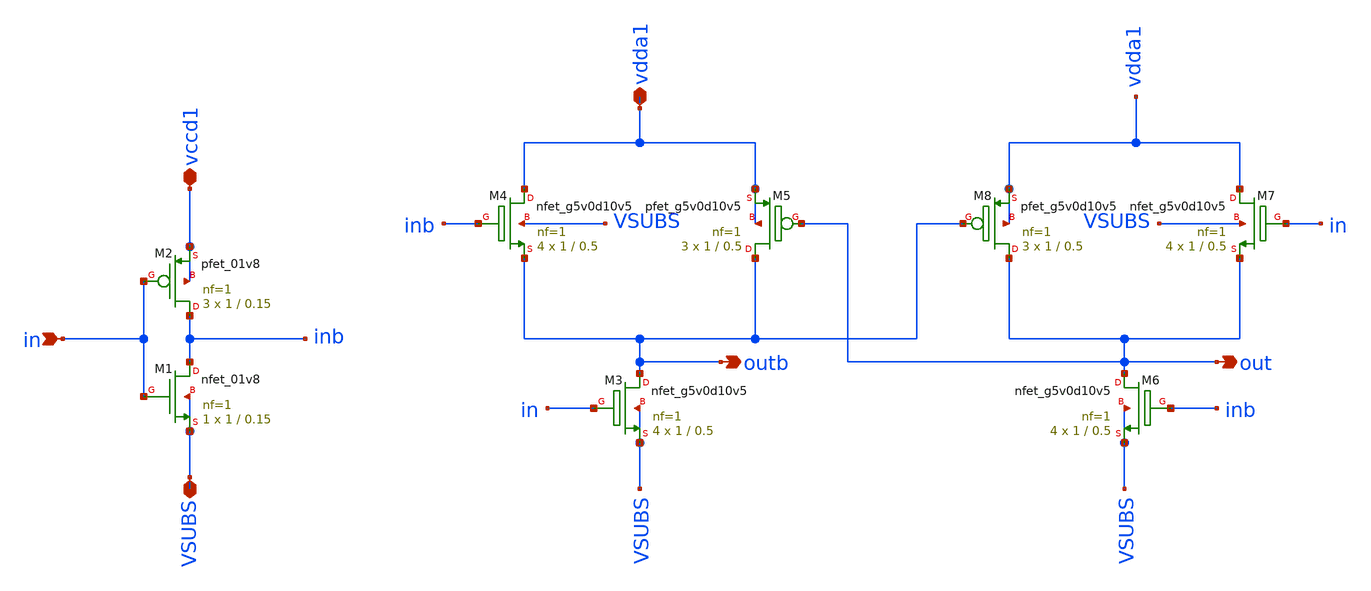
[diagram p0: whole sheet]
** sch_path: xschem/level_up_shifter_x4.sch
**.subckt level_up_shifter_x4 in vccd1 VSUBS vdda1 out outb
*.ipin in
*.iopin vccd1
*.iopin VSUBS
*.iopin vdda1
*.opin out
*.opin outb
XM1 inb in VSUBS VSUBS sky130_fd_pr__nfet_01v8 L=0.15 W=1 nf=1 ad='int((nf+1)/2) * W/nf * 0.29' as='int((nf+2)/2) * W/nf * 0.29'
+ pd='2*int((nf+1)/2) * (W/nf + 0.29)' ps='2*int((nf+2)/2) * (W/nf + 0.29)' nrd='0.29 / W' nrs='0.29 / W'
+ sa=0 sb=0 sd=0 mult=1 m=1
XM2 inb in vccd1 vccd1 sky130_fd_pr__pfet_01v8 L=0.15 W=1 nf=1 ad='int((nf+1)/2) * W/nf * 0.29' as='int((nf+2)/2) * W/nf * 0.29'
+ pd='2*int((nf+1)/2) * (W/nf + 0.29)' ps='2*int((nf+2)/2) * (W/nf + 0.29)' nrd='0.29 / W' nrs='0.29 / W'
+ sa=0 sb=0 sd=0 mult=3 m=3
XM3 outb in VSUBS VSUBS sky130_fd_pr__nfet_g5v0d10v5 L=0.5 W=1 nf=1 ad='int((nf+1)/2) * W/nf * 0.29'
+ as='int((nf+2)/2) * W/nf * 0.29' pd='2*int((nf+1)/2) * (W/nf + 0.29)' ps='2*int((nf+2)/2) * (W/nf + 0.29)'
+ nrd='0.29 / W' nrs='0.29 / W' sa=0 sb=0 sd=0 mult=4 m=4
XM4 vdda1 inb outb VSUBS sky130_fd_pr__nfet_g5v0d10v5 L=0.5 W=1 nf=1 ad='int((nf+1)/2) * W/nf * 0.29'
+ as='int((nf+2)/2) * W/nf * 0.29' pd='2*int((nf+1)/2) * (W/nf + 0.29)' ps='2*int((nf+2)/2) * (W/nf + 0.29)'
+ nrd='0.29 / W' nrs='0.29 / W' sa=0 sb=0 sd=0 mult=4 m=4
XM5 outb out vdda1 vdda1 sky130_fd_pr__pfet_g5v0d10v5 L=0.5 W=1 nf=1 ad='int((nf+1)/2) * W/nf * 0.29'
+ as='int((nf+2)/2) * W/nf * 0.29' pd='2*int((nf+1)/2) * (W/nf + 0.29)' ps='2*int((nf+2)/2) * (W/nf + 0.29)'
+ nrd='0.29 / W' nrs='0.29 / W' sa=0 sb=0 sd=0 mult=3 m=3
XM6 out inb VSUBS VSUBS sky130_fd_pr__nfet_g5v0d10v5 L=0.5 W=1 nf=1 ad='int((nf+1)/2) * W/nf * 0.29'
+ as='int((nf+2)/2) * W/nf * 0.29' pd='2*int((nf+1)/2) * (W/nf + 0.29)' ps='2*int((nf+2)/2) * (W/nf + 0.29)'
+ nrd='0.29 / W' nrs='0.29 / W' sa=0 sb=0 sd=0 mult=4 m=4
XM7 vdda1 in out VSUBS sky130_fd_pr__nfet_g5v0d10v5 L=0.5 W=1 nf=1 ad='int((nf+1)/2) * W/nf * 0.29' as='int((nf+2)/2) * W/nf * 0.29'
+ pd='2*int((nf+1)/2) * (W/nf + 0.29)' ps='2*int((nf+2)/2) * (W/nf + 0.29)' nrd='0.29 / W' nrs='0.29 / W'
+ sa=0 sb=0 sd=0 mult=4 m=4
XM8 out outb vdda1 vdda1 sky130_fd_pr__pfet_g5v0d10v5 L=0.5 W=1 nf=1 ad='int((nf+1)/2) * W/nf * 0.29'
+ as='int((nf+2)/2) * W/nf * 0.29' pd='2*int((nf+1)/2) * (W/nf + 0.29)' ps='2*int((nf+2)/2) * (W/nf + 0.29)'
+ nrd='0.29 / W' nrs='0.29 / W' sa=0 sb=0 sd=0 mult=3 m=3
**.ends
.end
